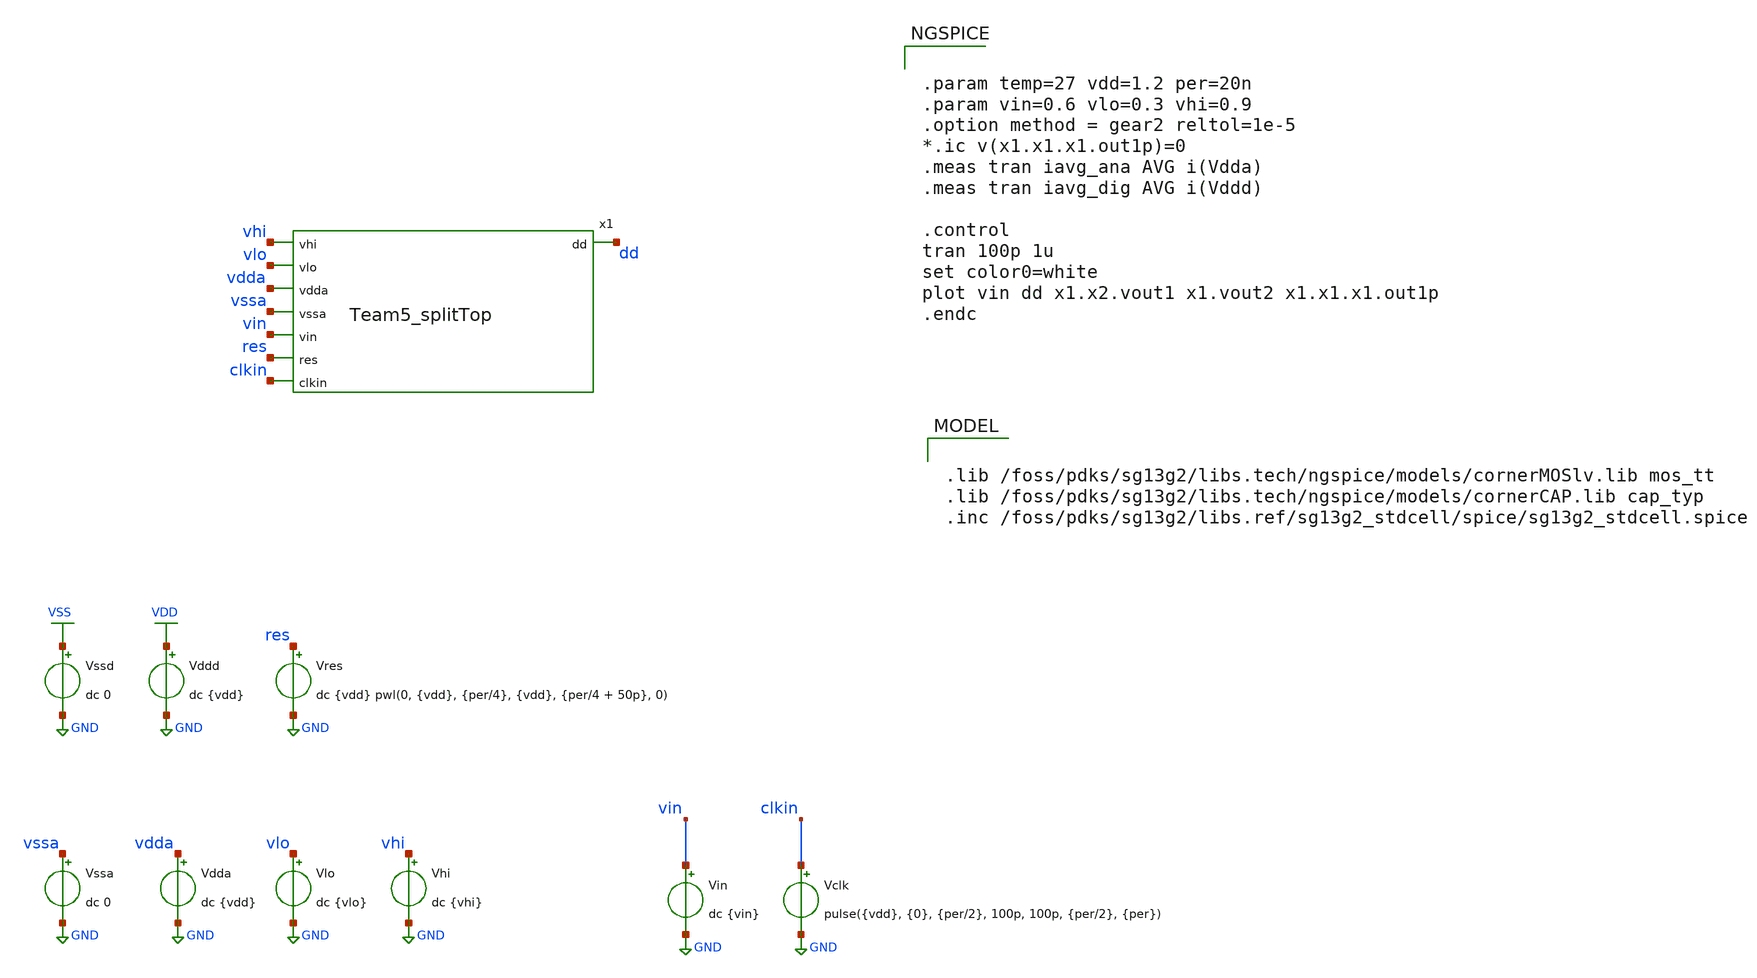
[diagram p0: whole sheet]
** sch_path: 5_Design/4_Layout/Team 5/splitUpSimulationsAndSchematics/Team5_splitTop_tb.sch
**.subckt Team5_splitTop_tb
Vssd VSS GND dc 0
Vddd VDD GND dc {vdd}
Vres res GND dc {vdd} pwl(0, {vdd}, {per/4}, {vdd}, {per/4 + 50p}, 0)
Vssa vssa GND dc 0
Vdda vdda GND dc {vdd}
Vlo vlo GND dc {vlo}
Vhi vhi GND dc {vhi}
Vin vin GND dc {vin}
Vclk clkin GND pulse({vdd}, {0}, {per/2}, 100p, 100p, {per/2}, {per})
x1 vhi vlo dd vdda vssa vin res clkin Team5_splitTop
**** begin user architecture code

.lib /foss/pdks/sg13g2/libs.tech/ngspice/models/cornerMOSlv.lib mos_tt
.lib /foss/pdks/sg13g2/libs.tech/ngspice/models/cornerCAP.lib cap_typ
.inc /foss/pdks/sg13g2/libs.ref/sg13g2_stdcell/spice/sg13g2_stdcell.spice



.param temp=27 vdd=1.2 per=20n
.param vin=0.6 vlo=0.3 vhi=0.9
.option method = gear2 reltol=1e-5
*.ic v(x1.x1.x1.out1p)=0
.meas tran iavg_ana AVG i(Vdda)
.meas tran iavg_dig AVG i(Vddd)

.control
tran 100p 1u
set color0=white
plot vin dd x1.x2.vout1 x1.vout2 x1.x1.x1.out1p
.endc


**** end user architecture code
**.ends
.GLOBAL GND
.GLOBAL VDD
.GLOBAL VSS
.end
